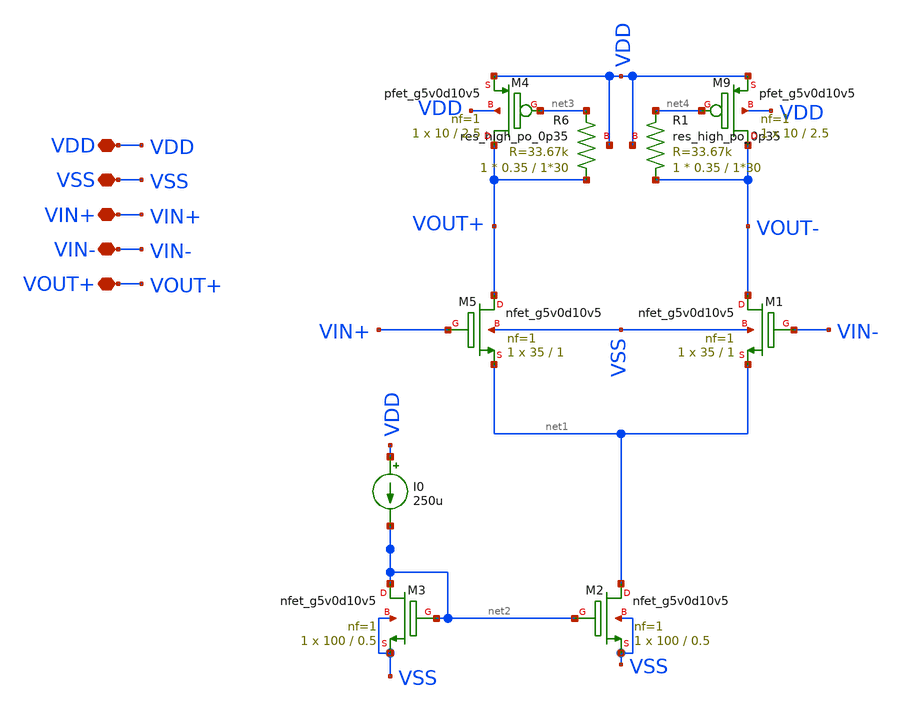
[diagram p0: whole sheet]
** sch_path: amplifiers/differencial_stage_amps/basic_stages/basic_NMOS_dif_stage/differential_stage.sch
**.subckt differential_stage VDD VSS VIN+ VIN- VOUT+
*.iopin VDD
*.iopin VSS
*.iopin VIN+
*.iopin VIN-
*.iopin VOUT+
XM5 VOUT+ VIN+ net1 VSS sky130_fd_pr__nfet_g5v0d10v5 L=1 W=35 nf=1 ad='int((1 + 1)/2) * 35 / 1 * 0.29'
+ as='int((1 + 2)/2) * 35 / 1 * 0.29' pd='2*int((1 + 1)/2) * (35 / 1 + 0.29)' ps='2*int((1 + 2)/2) * (35 / 1 + 0.29)'
+ nrd='0.29 / 35 ' nrs='0.29 / 35 ' sa=0 sb=0 sd=0 mult=1 m=1
XM1 VOUT- VIN- net1 VSS sky130_fd_pr__nfet_g5v0d10v5 L=1 W=35 nf=1 ad='int((1 + 1)/2) * 35 / 1 * 0.29'
+ as='int((1 + 2)/2) * 35 / 1 * 0.29' pd='2*int((1 + 1)/2) * (35 / 1 + 0.29)' ps='2*int((1 + 2)/2) * (35 / 1 + 0.29)'
+ nrd='0.29 / 35 ' nrs='0.29 / 35 ' sa=0 sb=0 sd=0 mult=1 m=1
XM2 net1 net2 VSS VSS sky130_fd_pr__nfet_g5v0d10v5 L=0.5 W=100 nf=1 ad='int((1 + 1)/2) * 100 / 1 * 0.29'
+ as='int((1 + 2)/2) * 100 / 1 * 0.29' pd='2*int((1 + 1)/2) * (100 / 1 + 0.29)' ps='2*int((1 + 2)/2) * (100 / 1 + 0.29)'
+ nrd='0.29 / 100 ' nrs='0.29 / 100 ' sa=0 sb=0 sd=0 mult=1 m=1
XM3 net2 net2 VSS VSS sky130_fd_pr__nfet_g5v0d10v5 L=0.5 W=100 nf=1 ad='int((1 + 1)/2) * 100 / 1 * 0.29'
+ as='int((1 + 2)/2) * 100 / 1 * 0.29' pd='2*int((1 + 1)/2) * (100 / 1 + 0.29)' ps='2*int((1 + 2)/2) * (100 / 1 + 0.29)'
+ nrd='0.29 / 100 ' nrs='0.29 / 100 ' sa=0 sb=0 sd=0 mult=1 m=1
I0 VDD net2 250u
XR6 VOUT+ net3 VDD sky130_fd_pr__res_high_po_0p35 L=1*30 mult=1 m=1
XR1 VOUT- net4 VDD sky130_fd_pr__res_high_po_0p35 L=1*30 mult=1 m=1
XM9 VOUT- net4 VDD VDD sky130_fd_pr__pfet_g5v0d10v5 L=2.5 W=10 nf=1 ad='int((1 + 1)/2) * 10 / 1 * 0.29'
+ as='int((1 + 2)/2) * 10 / 1 * 0.29' pd='2*int((1 + 1)/2) * (10 / 1 + 0.29)' ps='2*int((1 + 2)/2) * (10 / 1 + 0.29)'
+ nrd='0.29 / 10 ' nrs='0.29 / 10 ' sa=0 sb=0 sd=0 mult=1 m=1
XM4 VOUT+ net3 VDD VDD sky130_fd_pr__pfet_g5v0d10v5 L=2.5 W=10 nf=1 ad='int((1 + 1)/2) * 10 / 1 * 0.29'
+ as='int((1 + 2)/2) * 10 / 1 * 0.29' pd='2*int((1 + 1)/2) * (10 / 1 + 0.29)' ps='2*int((1 + 2)/2) * (10 / 1 + 0.29)'
+ nrd='0.29 / 10 ' nrs='0.29 / 10 ' sa=0 sb=0 sd=0 mult=1 m=1
**.ends
.end
